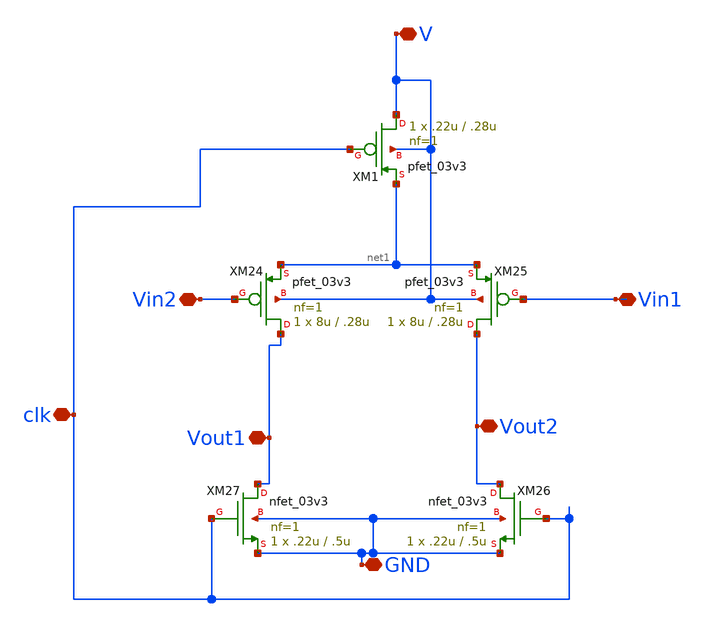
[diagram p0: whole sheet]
** sch_path: SAR_ADC/xschem/designs/preampp.sch
**.subckt preampp V GND Vout2 Vout1 clk Vin2 Vin1
*.iopin V
*.iopin GND
*.iopin Vout2
*.iopin Vout1
*.iopin clk
*.iopin Vin2
*.iopin Vin1
XM26 Vout2 clk GND GND nfet_03v3 L=.5u W=.22u nf=1 ad='int((nf+1)/2) * W/nf * 0.18u' as='int((nf+2)/2) * W/nf * 0.18u'
+ pd='2*int((nf+1)/2) * (W/nf + 0.18u)' ps='2*int((nf+2)/2) * (W/nf + 0.18u)' nrd='0.18u / W' nrs='0.18u / W'
+ sa=0 sb=0 sd=0 m=1
XM27 Vout1 clk GND GND nfet_03v3 L=.5u W=.22u nf=1 ad='int((nf+1)/2) * W/nf * 0.18u' as='int((nf+2)/2) * W/nf * 0.18u'
+ pd='2*int((nf+1)/2) * (W/nf + 0.18u)' ps='2*int((nf+2)/2) * (W/nf + 0.18u)' nrd='0.18u / W' nrs='0.18u / W'
+ sa=0 sb=0 sd=0 m=1
XM24 Vout1 Vin2 net1 V pfet_03v3 L=.28u W=8u nf=1 ad='int((nf+1)/2) * W/nf * 0.18u' as='int((nf+2)/2) * W/nf * 0.18u'
+ pd='2*int((nf+1)/2) * (W/nf + 0.18u)' ps='2*int((nf+2)/2) * (W/nf + 0.18u)' nrd='0.18u / W' nrs='0.18u / W'
+ sa=0 sb=0 sd=0 m=1
XM25 Vout2 Vin1 net1 V pfet_03v3 L=.28u W=8u nf=1 ad='int((nf+1)/2) * W/nf * 0.18u' as='int((nf+2)/2) * W/nf * 0.18u'
+ pd='2*int((nf+1)/2) * (W/nf + 0.18u)' ps='2*int((nf+2)/2) * (W/nf + 0.18u)' nrd='0.18u / W' nrs='0.18u / W'
+ sa=0 sb=0 sd=0 m=1
XM1 V clk net1 V pfet_03v3 L=.28u W=.22u nf=1 ad='int((nf+1)/2) * W/nf * 0.18u' as='int((nf+2)/2) * W/nf * 0.18u'
+ pd='2*int((nf+1)/2) * (W/nf + 0.18u)' ps='2*int((nf+2)/2) * (W/nf + 0.18u)' nrd='0.18u / W' nrs='0.18u / W'
+ sa=0 sb=0 sd=0 m=1
**.ends
.end
